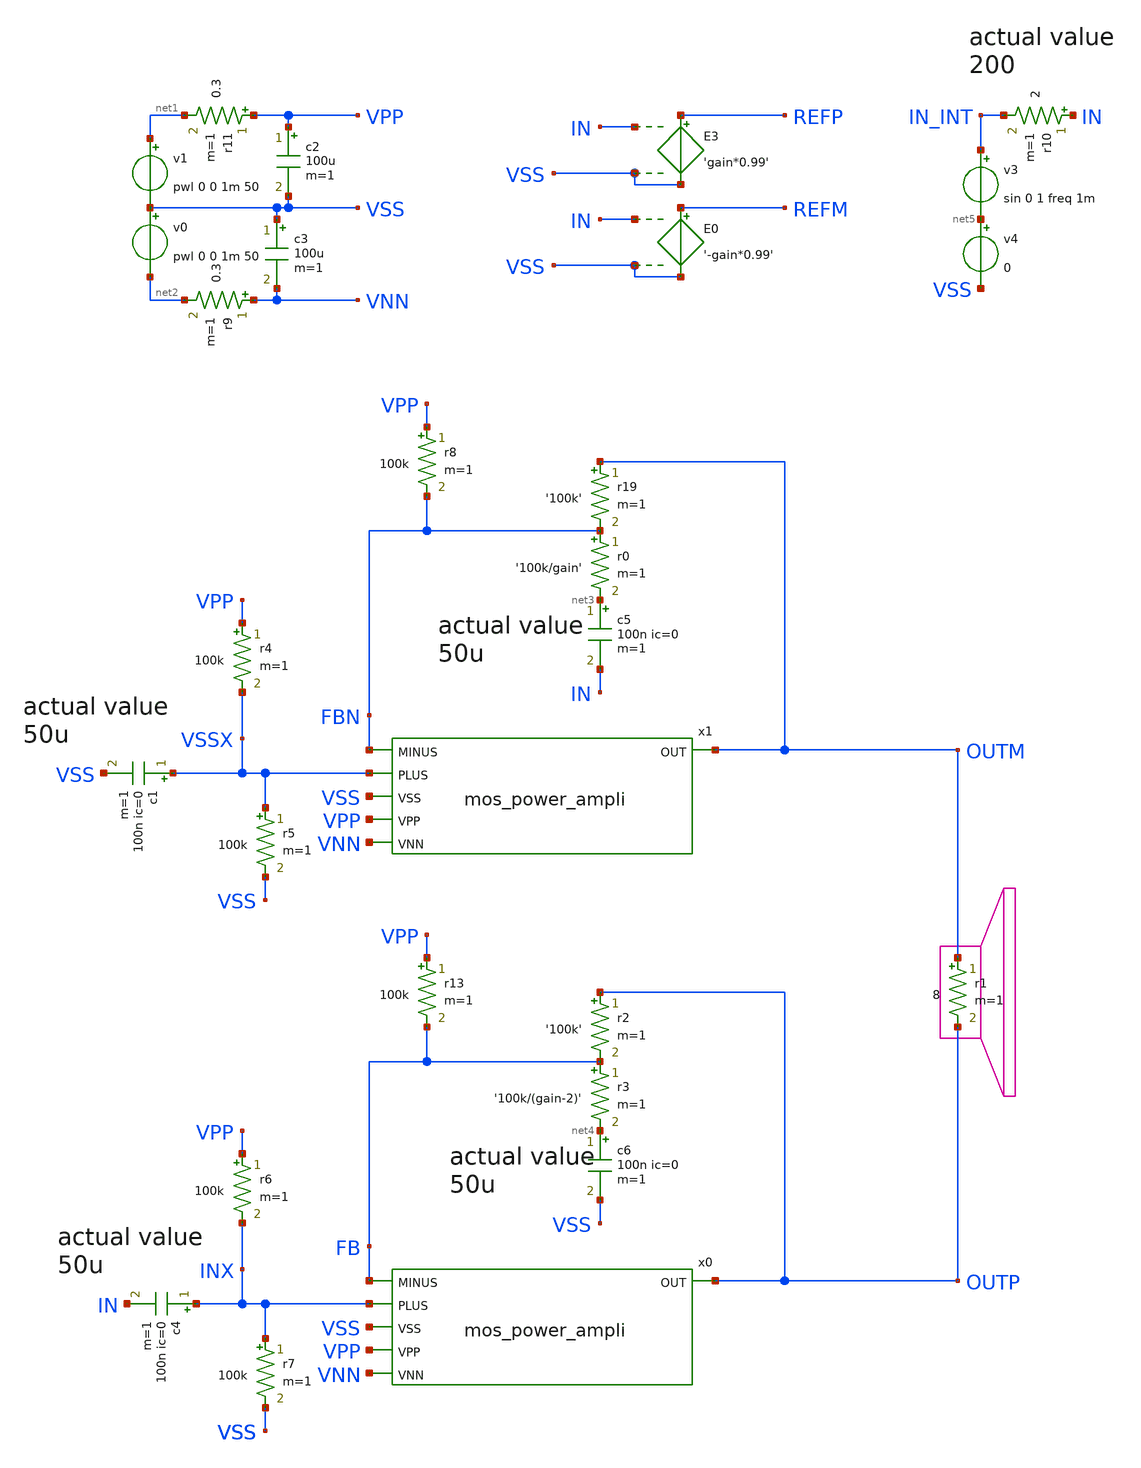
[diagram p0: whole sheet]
** sch_path: xschem_library/examples/poweramp.sch
**.subckt poweramp
v1 net1 VSS pwl 0 0 1m 50
v0 VSS net2 pwl 0 0 1m 50
r1 OUTM OUTP 8 m=1
E3 REFP VSS IN VSS 'gain*0.99'
c2 VPP VSS 100u m=1
c3 VSS VNN 100u m=1
r11 VPP net1 0.3 m=1
r9 VNN net2 0.3 m=1
r19 OUTM FBN '100k' m=1
r0 FBN net3 '100k/gain' m=1
x1 OUTM VSSX FBN VPP VNN VSS mos_power_ampli
x0 OUTP INX FB VPP VNN VSS mos_power_ampli
r6 VPP INX 100k m=1
r7 INX VSS 100k m=1
E0 REFM VSS IN VSS '-gain*0.99'
c5 net3 IN 100n ic=0 m=1
c6 net4 VSS 100n ic=0 m=1
r2 OUTP FB '100k' m=1
r3 FB net4 '100k/(gain-2)' m=1
v3 IN_INT net5 sin 0 1 freq 1m
r4 VPP VSSX 100k m=1
r5 VSSX VSS 100k m=1
r8 VPP FBN 100k m=1
c4 INX IN 100n ic=0 m=1
c1 VSSX VSS 100n ic=0 m=1
r10 IN IN_INT 2 m=1
r13 VPP FB 100k m=1
v4 net5 VSS 0
**** begin user architecture code

.option PARHIER=LOCAL RUNLVL=6 post MODMONTE=1 warn maxwarns=400
.option ITL4=20000 ITL5=0
* .option sampling_method = SRS
* .option method=gear
vvss vss 0 dc 0
.temp 30

.param freq=20k
.param gain=42
.tran '2m/freq' '1m + 160/freq' uic

** models are generally not free: you must download
** SPICE models for active devices and put them  into the below
** referenced file in netlist/simulation directory.
.include "models_poweramp.txt"
.save all
* .FOUR 20k v(outm,outp)
* .probe i(*)
* .probe p(r*) p(v*)


**** end user architecture code
**.ends
.end
